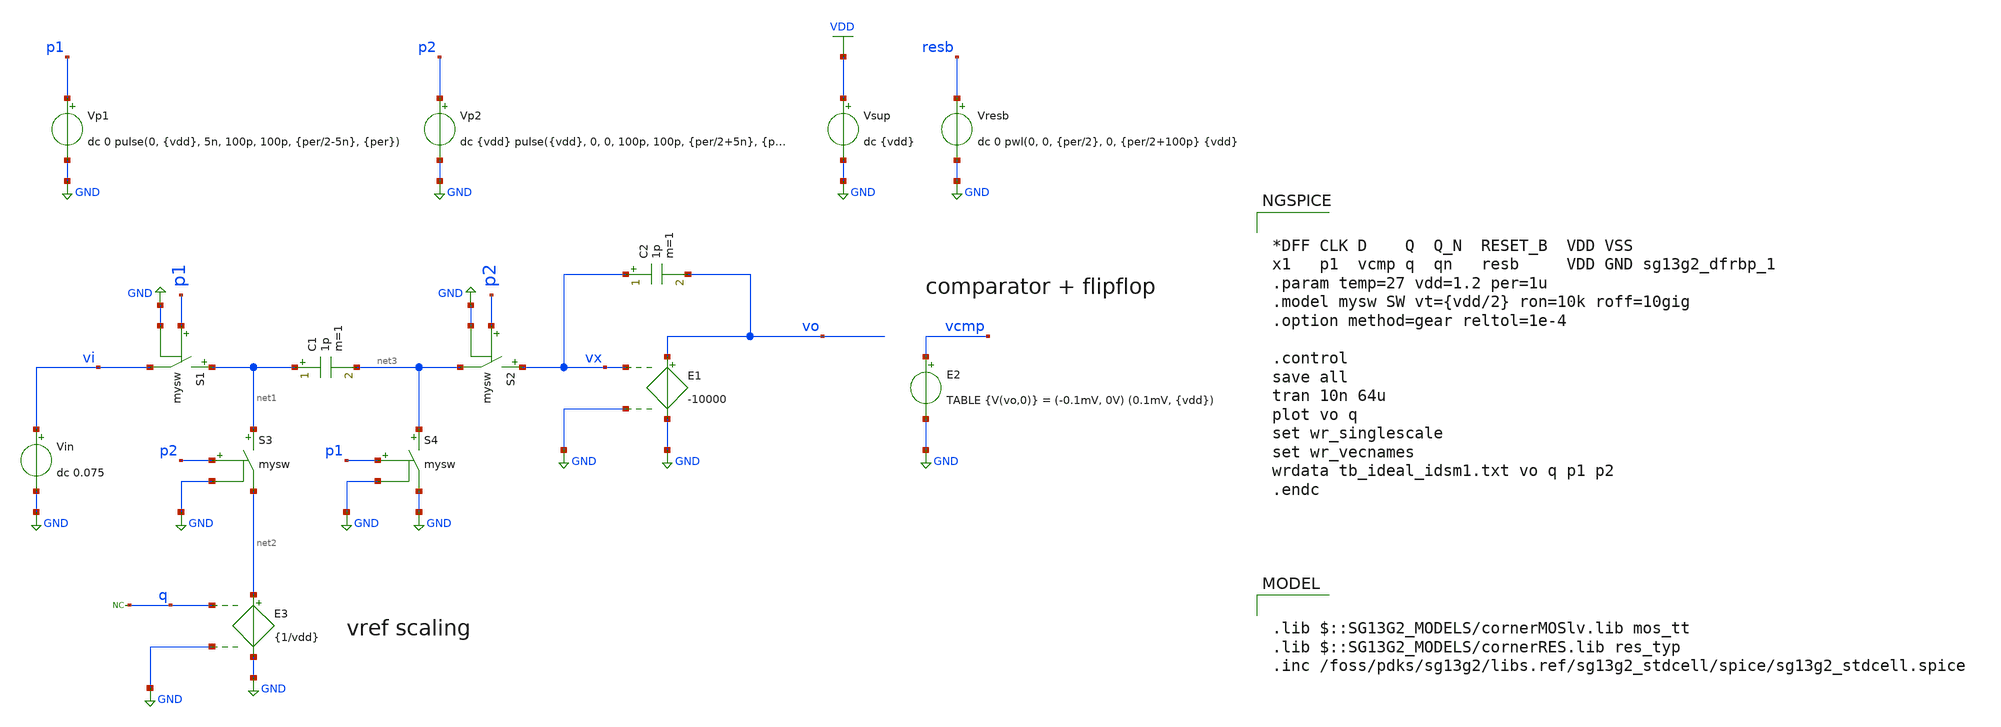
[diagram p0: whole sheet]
** sch_path: 5_Design/2_Idealized_circuits/tb_ideal_idsm1.sch
**.subckt tb_ideal_idsm1
Vp1 p1 GND dc 0 pulse(0, {vdd}, 5n, 100p, 100p, {per/2-5n}, {per})
E1 vo GND vx GND -10000
S1 net1 vi p1 GND mysw
Vp2 p2 GND dc {vdd} pulse({vdd}, 0, 0, 100p, 100p, {per/2+5n}, {per})
Vin vi GND dc 0.075
C1 net1 net3 1p m=1
S2 vx net3 p2 GND mysw
C2 vx vo 1p m=1
S3 net1 net2 p2 GND mysw
S4 net3 GND p1 GND mysw
E2 vcmp GND TABLE {V(vo,0)} = (-0.1mV, 0V) (0.1mV, {vdd})
Vsup VDD GND dc {vdd}
E3 net2 GND q GND {1/vdd}
Vresb resb GND dc 0 pwl(0, 0, {per/2}, 0, {per/2+100p} {vdd}
* noconn q
**** begin user architecture code

.lib $::SG13G2_MODELS/cornerMOSlv.lib mos_tt
.lib $::SG13G2_MODELS/cornerRES.lib res_typ
.inc /foss/pdks/sg13g2/libs.ref/sg13g2_stdcell/spice/sg13g2_stdcell.spice



*DFF CLK D    Q  Q_N  RESET_B  VDD VSS
x1   p1  vcmp q  qn   resb     VDD GND sg13g2_dfrbp_1
.param temp=27 vdd=1.2 per=1u
.model mysw SW vt={vdd/2} ron=10k roff=10gig
.option method=gear reltol=1e-4

.control
save all
tran 10n 64u
plot vo q
set wr_singlescale
set wr_vecnames
wrdata tb_ideal_idsm1.txt vo q p1 p2
.endc


**** end user architecture code
**.ends
.GLOBAL GND
.GLOBAL VDD
.end
